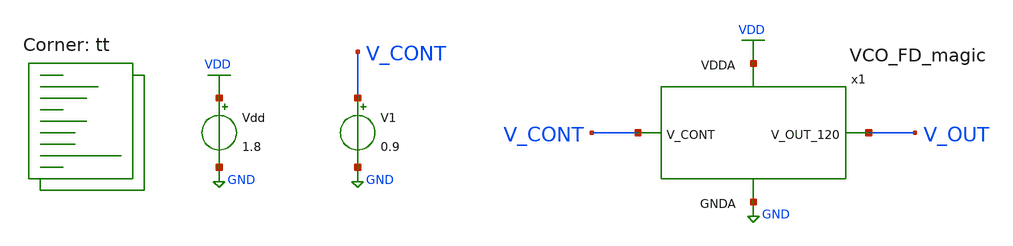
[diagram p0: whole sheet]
** sch_path: projects/pll/vco/magic/tb_current_starved_VCO_FD_magic.sch
**.subckt tb_current_starved_VCO_FD_magic
Vdd VDD GND 1.8
V1 V_CONT GND 0.9
x1 V_OUT VDD GND V_CONT VCO_FD_magic
**** begin user architecture code
.lib $::SKYWATER_MODELS/sky130.lib.spice tt



.include /foss/designs/my_design/projects/pll/vco/magic/VCO_FD_magic.spice
.include /foss/designs/my_design/projects/pll/vco/magic/current_starved_VCO_magic.spice
.include /foss/designs/my_design/projects/pll/divider/magic/divide_by_120/TSPC_FF_ratioed_divide120_magic.spice

.option method=gear
.option wnflag=1

.control

  let v_cont_start = 0.0
  let v_cont_stop = 1.9

  dowhile v_cont_start <= v_cont_stop
    alter v1 $&v_cont_start
    * save v(v_osc) v(v_cont) v(v_out)
    save all
    tran 5ps 30ns
    remzerovec
    write tb_current_starved_VCO_FD_magic_{$&v_cont_start}.raw
    * write tb_current_starved_VCO_FD_magic.raw
    linearize v(x1.v_osc.n0)
    let filename = v_cont_start * 100
    wrdata /foss/designs/my_design/projects/pll/vco/magic/tb_current_starved_VCO_FD_magic_{$&filename}.txt
+ v(x1.v_osc.n0)
    * wrdata /foss/designs/my_design/projects/pll/vco/magic/tb_current_starved_VCO_FD_magic.txt
+ v(x1.v_osc.n0)
    set appendwrite

    reset
    let v_cont_start = v_cont_start + 0.1
   end
.endc



**** end user architecture code
**.ends
.GLOBAL GND
.GLOBAL VDD
.end
